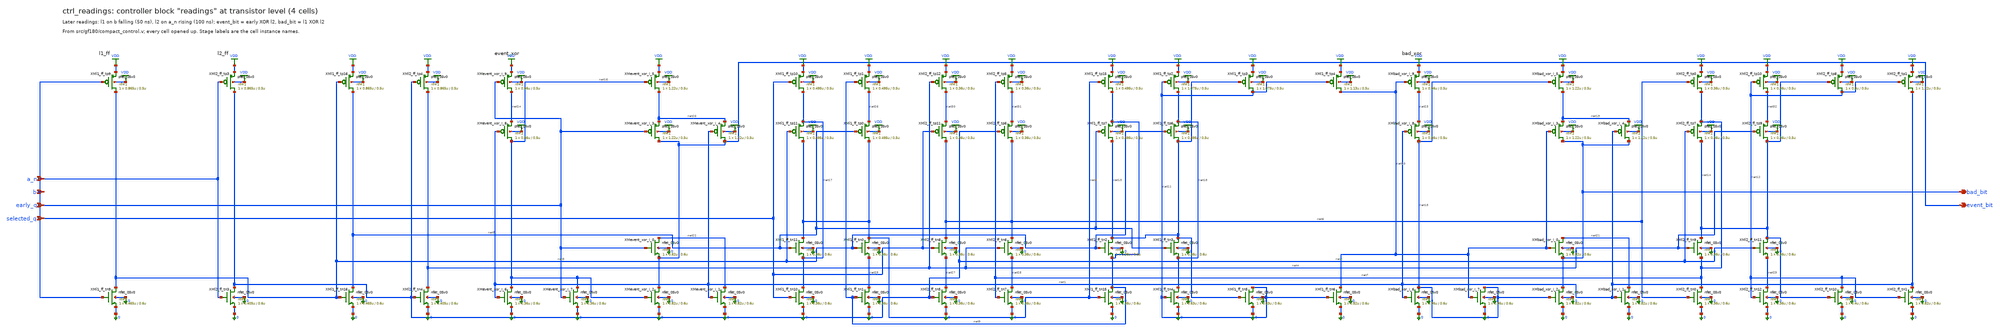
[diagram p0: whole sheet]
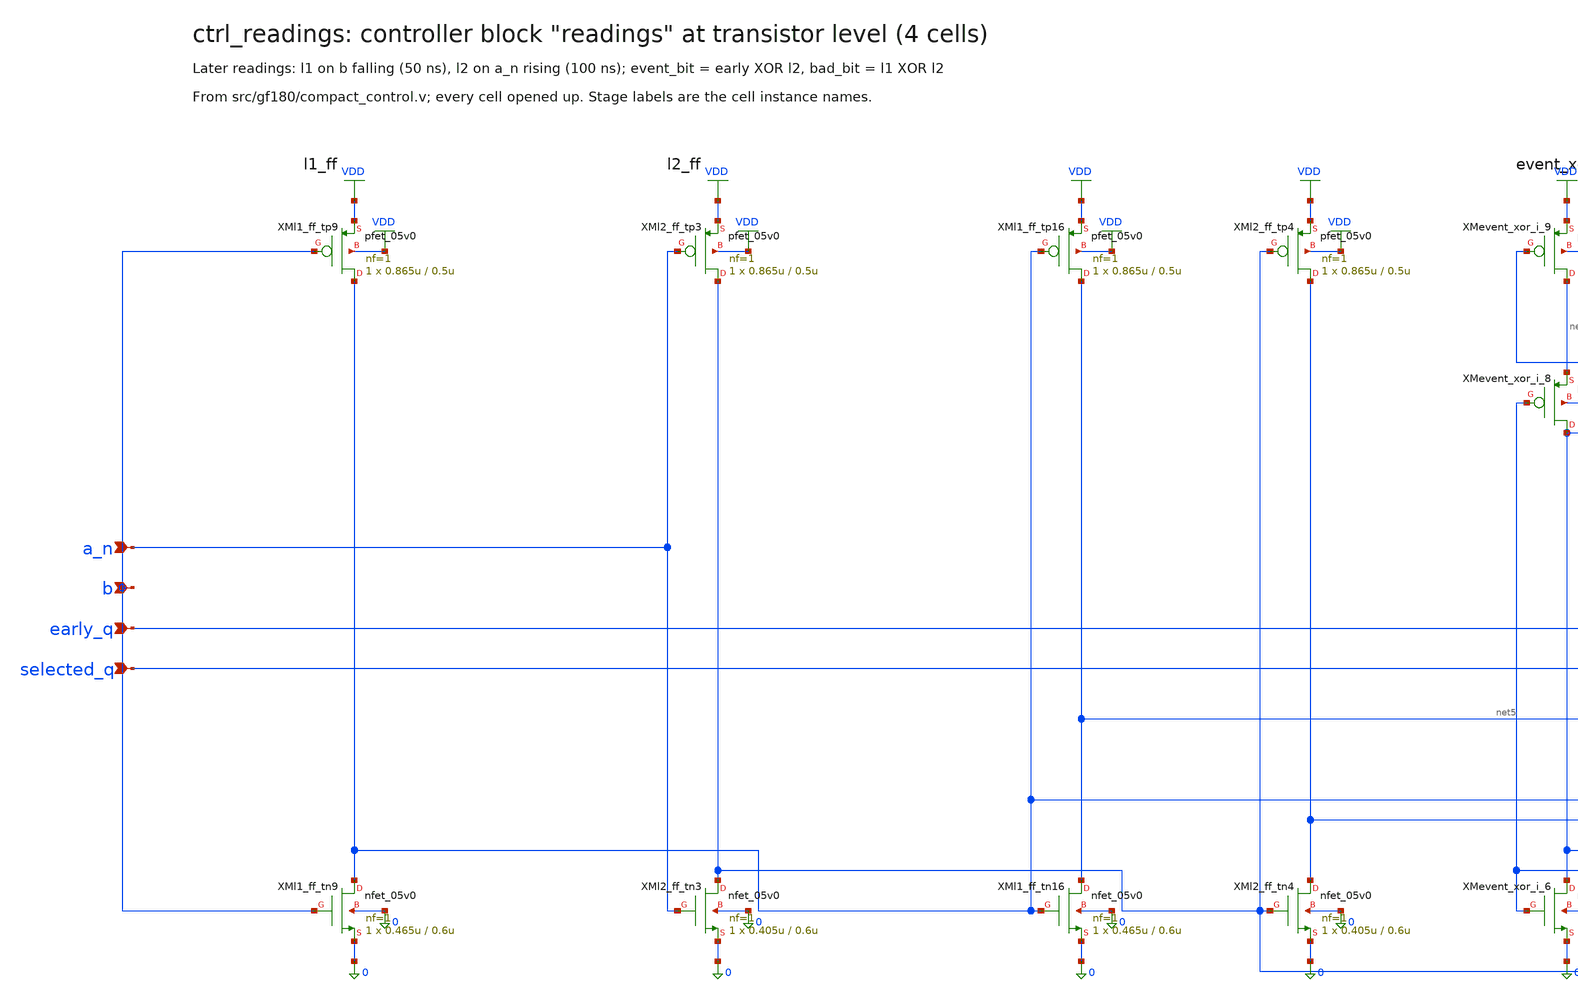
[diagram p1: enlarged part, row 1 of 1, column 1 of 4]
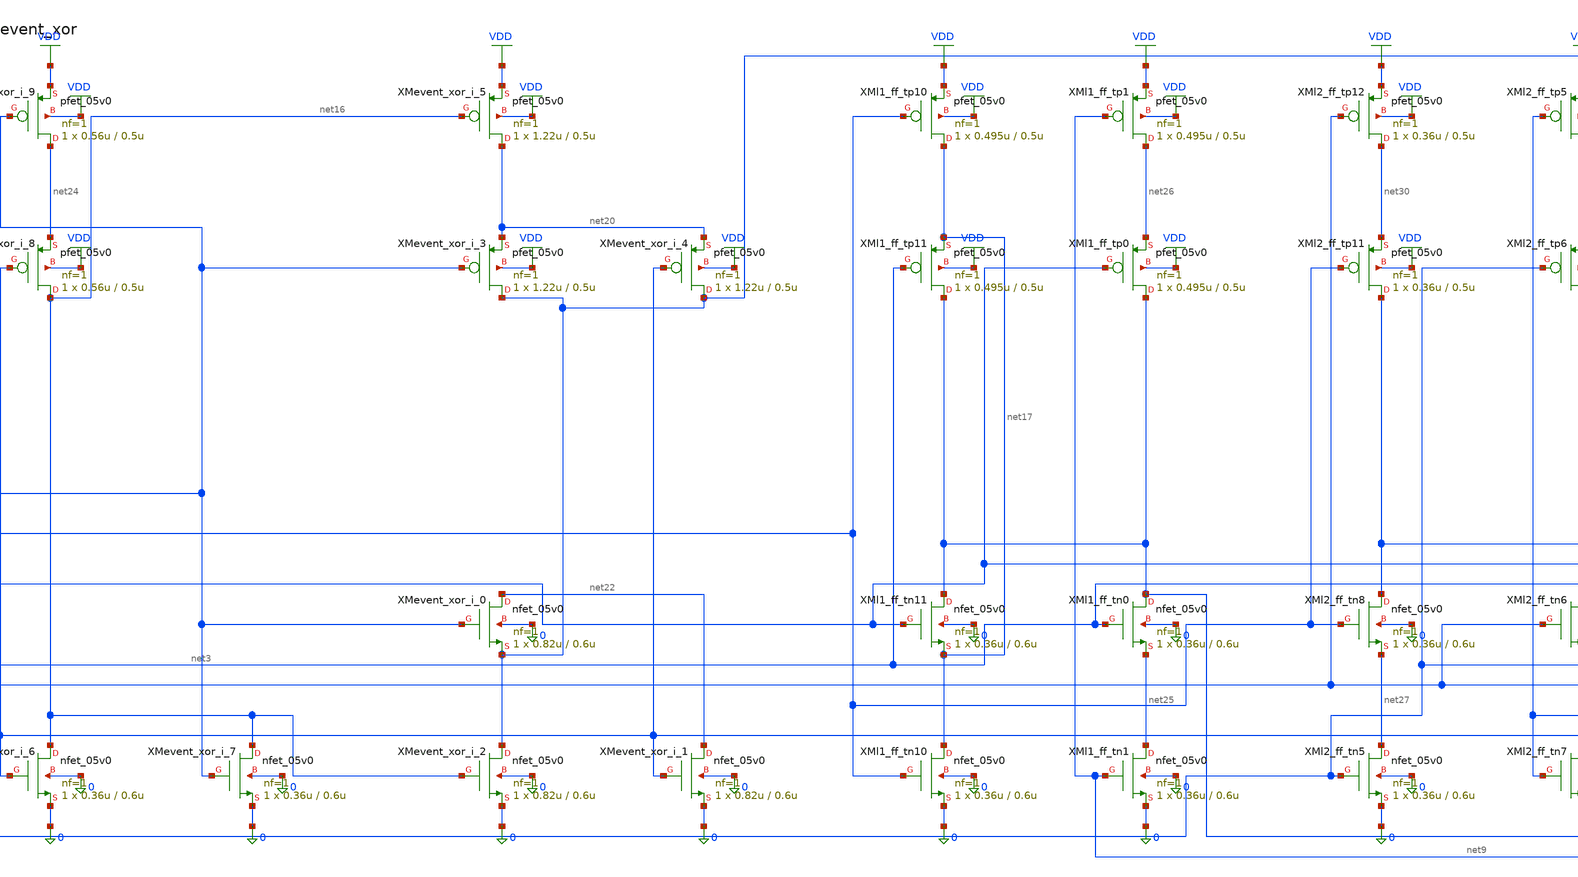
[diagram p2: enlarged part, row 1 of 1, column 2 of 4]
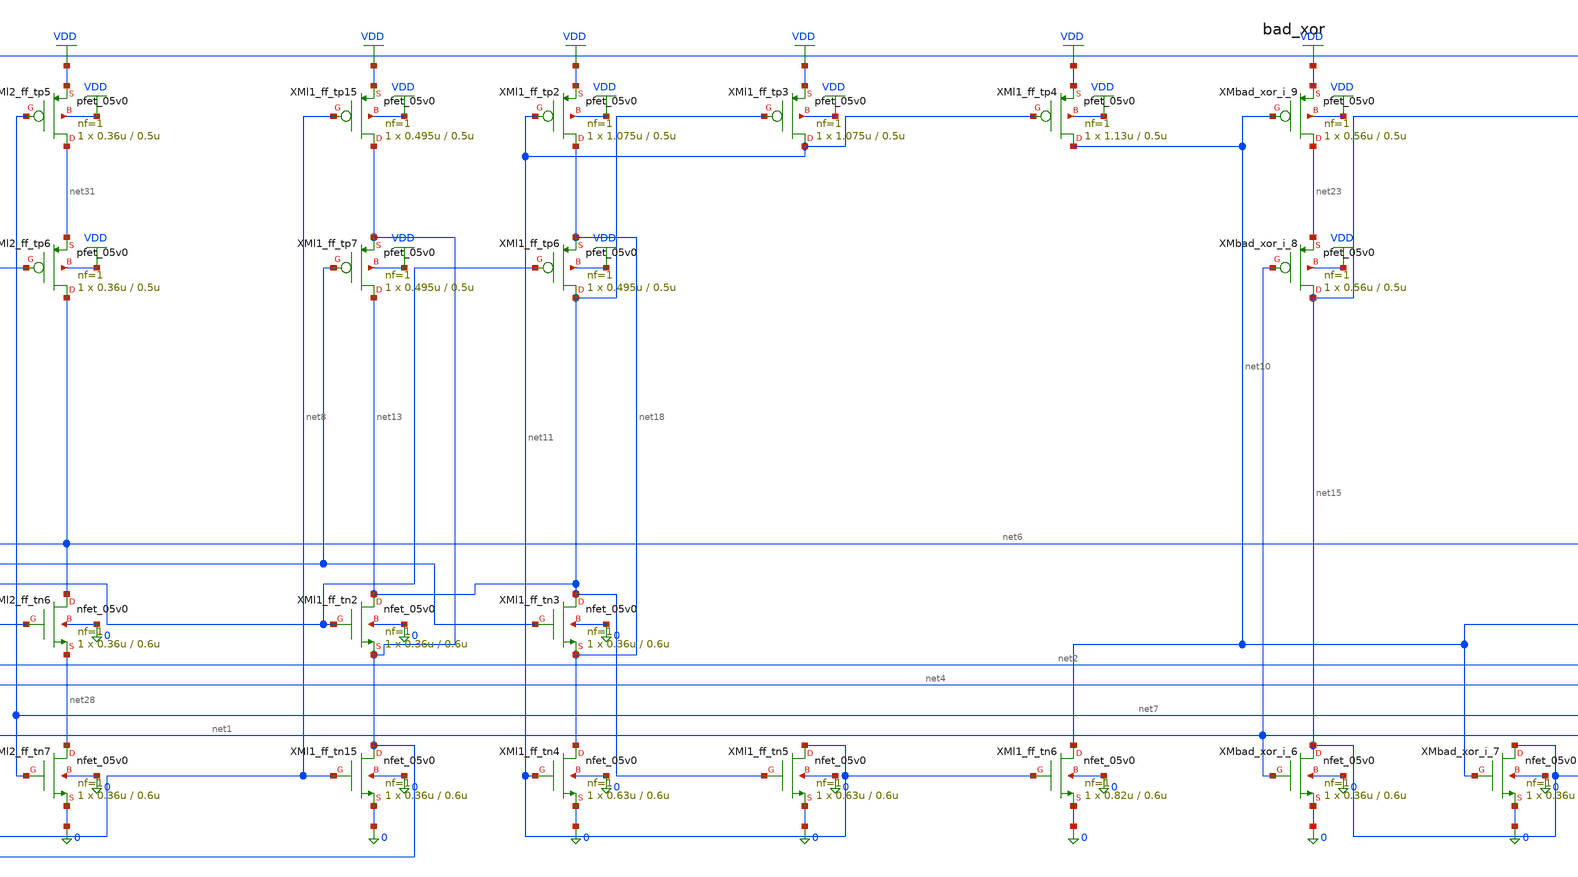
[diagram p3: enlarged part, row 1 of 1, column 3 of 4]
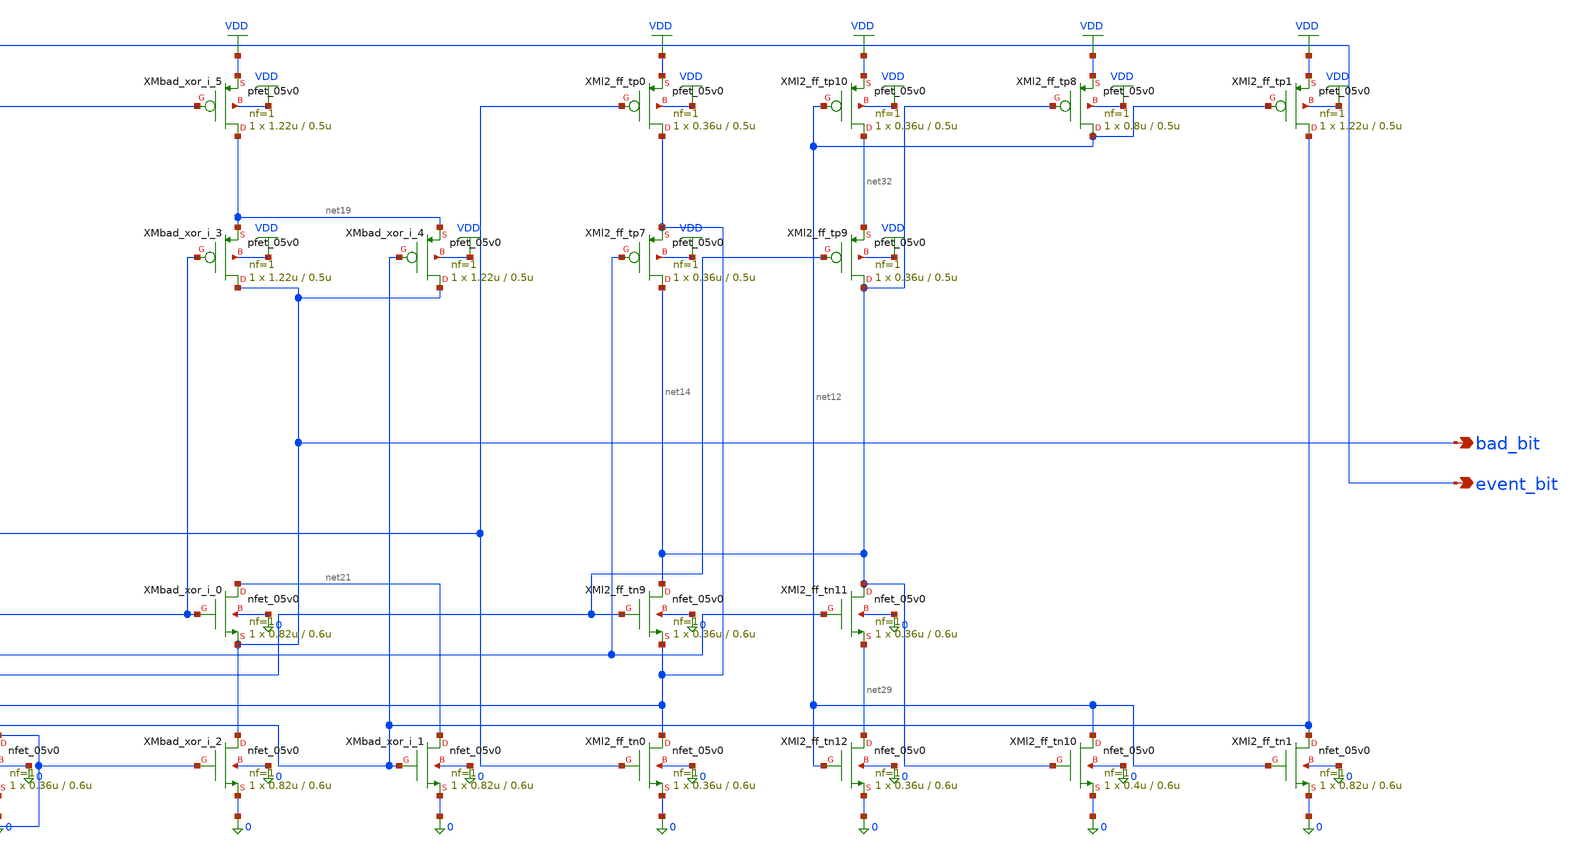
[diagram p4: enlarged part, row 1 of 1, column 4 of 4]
** sch_path: xschem/flat/ctrl_readings.sch
**.subckt ctrl_readings a_n b early_q selected_q bad_bit event_bit
*.ipin a_n
*.ipin b
*.ipin early_q
*.ipin selected_q
*.opin bad_bit
*.opin event_bit
XMbad_xor_i_6 net15 net1 0 0 nfet_05v0 L=0.6u W=0.36u nf=1 ad=1.8e-13 as=1.8e-13 pd=1.72e-06
+ ps=1.72e-06 nrd=0 nrs=0 sa=0 sb=0 sd=0 m=1
XMbad_xor_i_7 net15 net10 0 0 nfet_05v0 L=0.6u W=0.36u nf=1 ad=1.8e-13 as=1.8e-13 pd=1.72e-06
+ ps=1.72e-06 nrd=0 nrs=0 sa=0 sb=0 sd=0 m=1
XMbad_xor_i_2 bad_bit net15 0 0 nfet_05v0 L=0.6u W=0.82u nf=1 ad=4.1e-13 as=4.1e-13 pd=2.64e-06
+ ps=2.64e-06 nrd=0 nrs=0 sa=0 sb=0 sd=0 m=1
XMbad_xor_i_0 net21 net10 bad_bit 0 nfet_05v0 L=0.6u W=0.82u nf=1 ad=4.1e-13 as=4.1e-13 pd=2.64e-06
+ ps=2.64e-06 nrd=0 nrs=0 sa=0 sb=0 sd=0 m=1
XMbad_xor_i_1 net21 net1 0 0 nfet_05v0 L=0.6u W=0.82u nf=1 ad=4.1e-13 as=4.1e-13 pd=2.64e-06
+ ps=2.64e-06 nrd=0 nrs=0 sa=0 sb=0 sd=0 m=1
XMbad_xor_i_8 net15 net1 net23 VDD pfet_05v0 L=0.5u W=0.56u nf=1 ad=2.8e-13 as=2.8e-13 pd=2.12e-06
+ ps=2.12e-06 nrd=0 nrs=0 sa=0 sb=0 sd=0 m=1
XMbad_xor_i_9 net23 net10 VDD VDD pfet_05v0 L=0.5u W=0.56u nf=1 ad=2.8e-13 as=2.8e-13 pd=2.12e-06
+ ps=2.12e-06 nrd=0 nrs=0 sa=0 sb=0 sd=0 m=1
XMbad_xor_i_5 net19 net15 VDD VDD pfet_05v0 L=0.5u W=1.22u nf=1 ad=6.1e-13 as=6.1e-13 pd=3.44e-06
+ ps=3.44e-06 nrd=0 nrs=0 sa=0 sb=0 sd=0 m=1
XMbad_xor_i_3 bad_bit net10 net19 VDD pfet_05v0 L=0.5u W=1.22u nf=1 ad=6.1e-13 as=6.1e-13
+ pd=3.44e-06 ps=3.44e-06 nrd=0 nrs=0 sa=0 sb=0 sd=0 m=1
XMbad_xor_i_4 bad_bit net1 net19 VDD pfet_05v0 L=0.5u W=1.22u nf=1 ad=6.1e-13 as=6.1e-13 pd=3.44e-06
+ ps=3.44e-06 nrd=0 nrs=0 sa=0 sb=0 sd=0 m=1
XMevent_xor_i_6 net16 net1 0 0 nfet_05v0 L=0.6u W=0.36u nf=1 ad=1.8e-13 as=1.8e-13 pd=1.72e-06
+ ps=1.72e-06 nrd=0 nrs=0 sa=0 sb=0 sd=0 m=1
XMevent_xor_i_7 net16 early_q 0 0 nfet_05v0 L=0.6u W=0.36u nf=1 ad=1.8e-13 as=1.8e-13 pd=1.72e-06
+ ps=1.72e-06 nrd=0 nrs=0 sa=0 sb=0 sd=0 m=1
XMevent_xor_i_2 event_bit net16 0 0 nfet_05v0 L=0.6u W=0.82u nf=1 ad=4.1e-13 as=4.1e-13 pd=2.64e-06
+ ps=2.64e-06 nrd=0 nrs=0 sa=0 sb=0 sd=0 m=1
XMevent_xor_i_0 net22 early_q event_bit 0 nfet_05v0 L=0.6u W=0.82u nf=1 ad=4.1e-13 as=4.1e-13
+ pd=2.64e-06 ps=2.64e-06 nrd=0 nrs=0 sa=0 sb=0 sd=0 m=1
XMevent_xor_i_1 net22 net1 0 0 nfet_05v0 L=0.6u W=0.82u nf=1 ad=4.1e-13 as=4.1e-13 pd=2.64e-06
+ ps=2.64e-06 nrd=0 nrs=0 sa=0 sb=0 sd=0 m=1
XMevent_xor_i_8 net16 net1 net24 VDD pfet_05v0 L=0.5u W=0.56u nf=1 ad=2.8e-13 as=2.8e-13 pd=2.12e-06
+ ps=2.12e-06 nrd=0 nrs=0 sa=0 sb=0 sd=0 m=1
XMevent_xor_i_9 net24 early_q VDD VDD pfet_05v0 L=0.5u W=0.56u nf=1 ad=2.8e-13 as=2.8e-13
+ pd=2.12e-06 ps=2.12e-06 nrd=0 nrs=0 sa=0 sb=0 sd=0 m=1
XMevent_xor_i_5 net20 net16 VDD VDD pfet_05v0 L=0.5u W=1.22u nf=1 ad=6.1e-13 as=6.1e-13 pd=3.44e-06
+ ps=3.44e-06 nrd=0 nrs=0 sa=0 sb=0 sd=0 m=1
XMevent_xor_i_3 event_bit early_q net20 VDD pfet_05v0 L=0.5u W=1.22u nf=1 ad=6.1e-13 as=6.1e-13
+ pd=3.44e-06 ps=3.44e-06 nrd=0 nrs=0 sa=0 sb=0 sd=0 m=1
XMevent_xor_i_4 event_bit net1 net20 VDD pfet_05v0 L=0.5u W=1.22u nf=1 ad=6.1e-13 as=6.1e-13
+ pd=3.44e-06 ps=3.44e-06 nrd=0 nrs=0 sa=0 sb=0 sd=0 m=1
XMl1_ff_tn9 net3 b 0 0 nfet_05v0 L=0.6u W=0.465u nf=1 ad=2.325e-13 as=2.325e-13 pd=1.93e-06
+ ps=1.93e-06 nrd=0 nrs=0 sa=0 sb=0 sd=0 m=1
XMl1_ff_tn16 net5 net3 0 0 nfet_05v0 L=0.6u W=0.465u nf=1 ad=2.325e-13 as=2.325e-13 pd=1.93e-06
+ ps=1.93e-06 nrd=0 nrs=0 sa=0 sb=0 sd=0 m=1
XMl1_ff_tn10 net17 selected_q 0 0 nfet_05v0 L=0.6u W=0.36u nf=1 ad=1.8e-13 as=1.8e-13 pd=1.72e-06
+ ps=1.72e-06 nrd=0 nrs=0 sa=0 sb=0 sd=0 m=1
XMl1_ff_tn11 net8 net5 net17 0 nfet_05v0 L=0.6u W=0.36u nf=1 ad=1.8e-13 as=1.8e-13 pd=1.72e-06
+ ps=1.72e-06 nrd=0 nrs=0 sa=0 sb=0 sd=0 m=1
XMl1_ff_tn0 net8 net3 net25 0 nfet_05v0 L=0.6u W=0.36u nf=1 ad=1.8e-13 as=1.8e-13 pd=1.72e-06
+ ps=1.72e-06 nrd=0 nrs=0 sa=0 sb=0 sd=0 m=1
XMl1_ff_tn1 net25 net9 0 0 nfet_05v0 L=0.6u W=0.36u nf=1 ad=1.8e-13 as=1.8e-13 pd=1.72e-06
+ ps=1.72e-06 nrd=0 nrs=0 sa=0 sb=0 sd=0 m=1
XMl1_ff_tn15 net9 net8 0 0 nfet_05v0 L=0.6u W=0.36u nf=1 ad=1.8e-13 as=1.8e-13 pd=1.72e-06
+ ps=1.72e-06 nrd=0 nrs=0 sa=0 sb=0 sd=0 m=1
XMl1_ff_tn2 net13 net3 net9 0 nfet_05v0 L=0.6u W=0.36u nf=1 ad=1.8e-13 as=1.8e-13 pd=1.72e-06
+ ps=1.72e-06 nrd=0 nrs=0 sa=0 sb=0 sd=0 m=1
XMl1_ff_tn3 net13 net5 net18 0 nfet_05v0 L=0.6u W=0.36u nf=1 ad=1.8e-13 as=1.8e-13 pd=1.72e-06
+ ps=1.72e-06 nrd=0 nrs=0 sa=0 sb=0 sd=0 m=1
XMl1_ff_tn4 net18 net11 0 0 nfet_05v0 L=0.6u W=0.63u nf=1 ad=3.15e-13 as=3.15e-13 pd=2.26e-06
+ ps=2.26e-06 nrd=0 nrs=0 sa=0 sb=0 sd=0 m=1
XMl1_ff_tn5 net11 net13 0 0 nfet_05v0 L=0.6u W=0.63u nf=1 ad=3.15e-13 as=3.15e-13 pd=2.26e-06
+ ps=2.26e-06 nrd=0 nrs=0 sa=0 sb=0 sd=0 m=1
XMl1_ff_tn6 net10 net11 0 0 nfet_05v0 L=0.6u W=0.82u nf=1 ad=4.1e-13 as=4.1e-13 pd=2.64e-06
+ ps=2.64e-06 nrd=0 nrs=0 sa=0 sb=0 sd=0 m=1
XMl1_ff_tp9 net3 b VDD VDD pfet_05v0 L=0.5u W=0.865u nf=1 ad=4.325e-13 as=4.325e-13 pd=2.73e-06
+ ps=2.73e-06 nrd=0 nrs=0 sa=0 sb=0 sd=0 m=1
XMl1_ff_tp16 net5 net3 VDD VDD pfet_05v0 L=0.5u W=0.865u nf=1 ad=4.325e-13 as=4.325e-13 pd=2.73e-06
+ ps=2.73e-06 nrd=0 nrs=0 sa=0 sb=0 sd=0 m=1
XMl1_ff_tp10 net17 selected_q VDD VDD pfet_05v0 L=0.5u W=0.495u nf=1 ad=2.475e-13 as=2.475e-13
+ pd=1.99e-06 ps=1.99e-06 nrd=0 nrs=0 sa=0 sb=0 sd=0 m=1
XMl1_ff_tp11 net8 net3 net17 VDD pfet_05v0 L=0.5u W=0.495u nf=1 ad=2.475e-13 as=2.475e-13
+ pd=1.99e-06 ps=1.99e-06 nrd=0 nrs=0 sa=0 sb=0 sd=0 m=1
XMl1_ff_tp0 net8 net5 net26 VDD pfet_05v0 L=0.5u W=0.495u nf=1 ad=2.475e-13 as=2.475e-13 pd=1.99e-06
+ ps=1.99e-06 nrd=0 nrs=0 sa=0 sb=0 sd=0 m=1
XMl1_ff_tp1 net26 net9 VDD VDD pfet_05v0 L=0.5u W=0.495u nf=1 ad=2.475e-13 as=2.475e-13 pd=1.99e-06
+ ps=1.99e-06 nrd=0 nrs=0 sa=0 sb=0 sd=0 m=1
XMl1_ff_tp15 net9 net8 VDD VDD pfet_05v0 L=0.5u W=0.495u nf=1 ad=2.475e-13 as=2.475e-13 pd=1.99e-06
+ ps=1.99e-06 nrd=0 nrs=0 sa=0 sb=0 sd=0 m=1
XMl1_ff_tp7 net13 net5 net9 VDD pfet_05v0 L=0.5u W=0.495u nf=1 ad=2.475e-13 as=2.475e-13 pd=1.99e-06
+ ps=1.99e-06 nrd=0 nrs=0 sa=0 sb=0 sd=0 m=1
XMl1_ff_tp6 net13 net3 net18 VDD pfet_05v0 L=0.5u W=0.495u nf=1 ad=2.475e-13 as=2.475e-13
+ pd=1.99e-06 ps=1.99e-06 nrd=0 nrs=0 sa=0 sb=0 sd=0 m=1
XMl1_ff_tp2 net18 net11 VDD VDD pfet_05v0 L=0.5u W=1.075u nf=1 ad=5.375e-13 as=5.375e-13 pd=3.15e-06
+ ps=3.15e-06 nrd=0 nrs=0 sa=0 sb=0 sd=0 m=1
XMl1_ff_tp3 net11 net13 VDD VDD pfet_05v0 L=0.5u W=1.075u nf=1 ad=5.375e-13 as=5.375e-13 pd=3.15e-06
+ ps=3.15e-06 nrd=0 nrs=0 sa=0 sb=0 sd=0 m=1
XMl1_ff_tp4 net10 net11 VDD VDD pfet_05v0 L=0.5u W=1.13u nf=1 ad=5.65e-13 as=5.65e-13 pd=3.26e-06
+ ps=3.26e-06 nrd=0 nrs=0 sa=0 sb=0 sd=0 m=1
XMl2_ff_tn3 net2 a_n 0 0 nfet_05v0 L=0.6u W=0.405u nf=1 ad=2.025e-13 as=2.025e-13 pd=1.81e-06
+ ps=1.81e-06 nrd=0 nrs=0 sa=0 sb=0 sd=0 m=1
XMl2_ff_tn4 net4 net2 0 0 nfet_05v0 L=0.6u W=0.405u nf=1 ad=2.025e-13 as=2.025e-13 pd=1.81e-06
+ ps=1.81e-06 nrd=0 nrs=0 sa=0 sb=0 sd=0 m=1
XMl2_ff_tn5 net27 net2 0 0 nfet_05v0 L=0.6u W=0.36u nf=1 ad=1.8e-13 as=1.8e-13 pd=1.72e-06
+ ps=1.72e-06 nrd=0 nrs=0 sa=0 sb=0 sd=0 m=1
XMl2_ff_tn8 net6 selected_q net27 0 nfet_05v0 L=0.6u W=0.36u nf=1 ad=1.8e-13 as=1.8e-13 pd=1.72e-06
+ ps=1.72e-06 nrd=0 nrs=0 sa=0 sb=0 sd=0 m=1
XMl2_ff_tn6 net6 net4 net28 0 nfet_05v0 L=0.6u W=0.36u nf=1 ad=1.8e-13 as=1.8e-13 pd=1.72e-06
+ ps=1.72e-06 nrd=0 nrs=0 sa=0 sb=0 sd=0 m=1
XMl2_ff_tn7 net28 net7 0 0 nfet_05v0 L=0.6u W=0.36u nf=1 ad=1.8e-13 as=1.8e-13 pd=1.72e-06
+ ps=1.72e-06 nrd=0 nrs=0 sa=0 sb=0 sd=0 m=1
XMl2_ff_tn0 net7 net6 0 0 nfet_05v0 L=0.6u W=0.36u nf=1 ad=1.8e-13 as=1.8e-13 pd=1.72e-06
+ ps=1.72e-06 nrd=0 nrs=0 sa=0 sb=0 sd=0 m=1
XMl2_ff_tn9 net14 net4 net7 0 nfet_05v0 L=0.6u W=0.36u nf=1 ad=1.8e-13 as=1.8e-13 pd=1.72e-06
+ ps=1.72e-06 nrd=0 nrs=0 sa=0 sb=0 sd=0 m=1
XMl2_ff_tn11 net14 net2 net29 0 nfet_05v0 L=0.6u W=0.36u nf=1 ad=1.8e-13 as=1.8e-13 pd=1.72e-06
+ ps=1.72e-06 nrd=0 nrs=0 sa=0 sb=0 sd=0 m=1
XMl2_ff_tn12 net29 net12 0 0 nfet_05v0 L=0.6u W=0.36u nf=1 ad=1.8e-13 as=1.8e-13 pd=1.72e-06
+ ps=1.72e-06 nrd=0 nrs=0 sa=0 sb=0 sd=0 m=1
XMl2_ff_tn10 net12 net14 0 0 nfet_05v0 L=0.6u W=0.4u nf=1 ad=2e-13 as=2e-13 pd=1.8e-06 ps=1.8e-06
+ nrd=0 nrs=0 sa=0 sb=0 sd=0 m=1
XMl2_ff_tn1 net1 net12 0 0 nfet_05v0 L=0.6u W=0.82u nf=1 ad=4.1e-13 as=4.1e-13 pd=2.64e-06
+ ps=2.64e-06 nrd=0 nrs=0 sa=0 sb=0 sd=0 m=1
XMl2_ff_tp3 net2 a_n VDD VDD pfet_05v0 L=0.5u W=0.865u nf=1 ad=4.325e-13 as=4.325e-13 pd=2.73e-06
+ ps=2.73e-06 nrd=0 nrs=0 sa=0 sb=0 sd=0 m=1
XMl2_ff_tp4 net4 net2 VDD VDD pfet_05v0 L=0.5u W=0.865u nf=1 ad=4.325e-13 as=4.325e-13 pd=2.73e-06
+ ps=2.73e-06 nrd=0 nrs=0 sa=0 sb=0 sd=0 m=1
XMl2_ff_tp12 net30 net4 VDD VDD pfet_05v0 L=0.5u W=0.36u nf=1 ad=1.8e-13 as=1.8e-13 pd=1.72e-06
+ ps=1.72e-06 nrd=0 nrs=0 sa=0 sb=0 sd=0 m=1
XMl2_ff_tp11 net6 selected_q net30 VDD pfet_05v0 L=0.5u W=0.36u nf=1 ad=1.8e-13 as=1.8e-13
+ pd=1.72e-06 ps=1.72e-06 nrd=0 nrs=0 sa=0 sb=0 sd=0 m=1
XMl2_ff_tp6 net6 net2 net31 VDD pfet_05v0 L=0.5u W=0.36u nf=1 ad=1.8e-13 as=1.8e-13 pd=1.72e-06
+ ps=1.72e-06 nrd=0 nrs=0 sa=0 sb=0 sd=0 m=1
XMl2_ff_tp5 net31 net7 VDD VDD pfet_05v0 L=0.5u W=0.36u nf=1 ad=1.8e-13 as=1.8e-13 pd=1.72e-06
+ ps=1.72e-06 nrd=0 nrs=0 sa=0 sb=0 sd=0 m=1
XMl2_ff_tp0 net7 net6 VDD VDD pfet_05v0 L=0.5u W=0.36u nf=1 ad=1.8e-13 as=1.8e-13 pd=1.72e-06
+ ps=1.72e-06 nrd=0 nrs=0 sa=0 sb=0 sd=0 m=1
XMl2_ff_tp7 net14 net2 net7 VDD pfet_05v0 L=0.5u W=0.36u nf=1 ad=1.8e-13 as=1.8e-13 pd=1.72e-06
+ ps=1.72e-06 nrd=0 nrs=0 sa=0 sb=0 sd=0 m=1
XMl2_ff_tp9 net14 net4 net32 VDD pfet_05v0 L=0.5u W=0.36u nf=1 ad=1.8e-13 as=1.8e-13 pd=1.72e-06
+ ps=1.72e-06 nrd=0 nrs=0 sa=0 sb=0 sd=0 m=1
XMl2_ff_tp10 net32 net12 VDD VDD pfet_05v0 L=0.5u W=0.36u nf=1 ad=1.8e-13 as=1.8e-13 pd=1.72e-06
+ ps=1.72e-06 nrd=0 nrs=0 sa=0 sb=0 sd=0 m=1
XMl2_ff_tp8 net12 net14 VDD VDD pfet_05v0 L=0.5u W=0.8u nf=1 ad=4e-13 as=4e-13 pd=2.6e-06 ps=2.6e-06
+ nrd=0 nrs=0 sa=0 sb=0 sd=0 m=1
XMl2_ff_tp1 net1 net12 VDD VDD pfet_05v0 L=0.5u W=1.22u nf=1 ad=6.1e-13 as=6.1e-13 pd=3.44e-06
+ ps=3.44e-06 nrd=0 nrs=0 sa=0 sb=0 sd=0 m=1
**.ends
.GLOBAL VDD
.end
